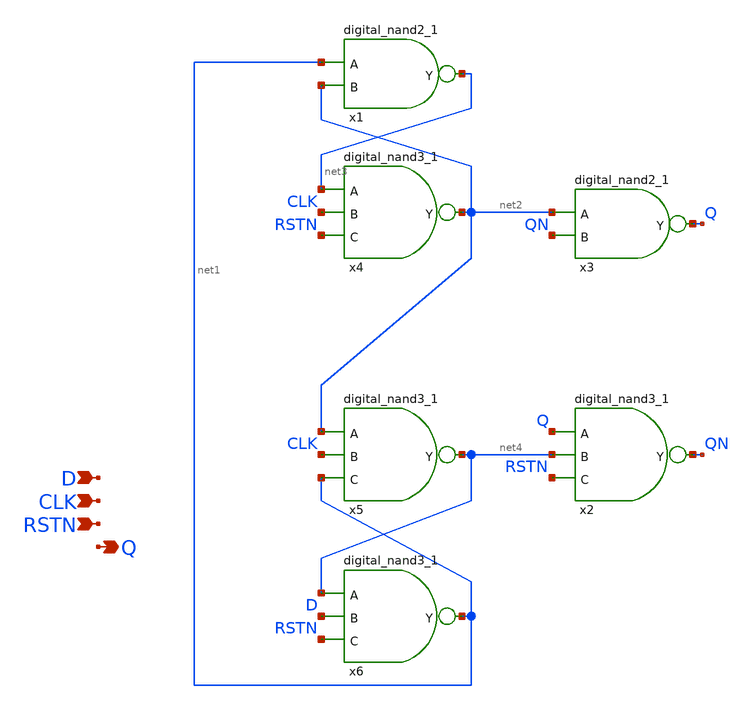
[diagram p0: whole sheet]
** sch_path: designs/libs/core_analog/digital/digital_dff.sch
**.subckt digital_dff D CLK Q RSTN
*.ipin D
*.ipin CLK
*.opin Q
*.ipin RSTN
x1 net1 net2 VDD VSS net3 digital_nand2_1
x3 net2 QN VDD VSS Q digital_nand2_1
x2 Q net4 RSTN VDD VSS QN digital_nand3_1
x4 net3 CLK RSTN VDD VSS net2 digital_nand3_1
x5 net2 CLK net1 VDD VSS net4 digital_nand3_1
x6 net4 D RSTN VDD VSS net1 digital_nand3_1
**.ends

* expanding   symbol:
*+  /foss/designs/sscs-chipathon2025-LNA/designs/libs/core_analog/digital/digital_nand2_1.sym # of pins=3
** sym_path: designs/libs/core_analog/digital/digital_nand2_1.sym
** sch_path: designs/libs/core_analog/digital/digital_nand2_1.sch
.subckt digital_nand2_1 A B VDD VSS Y
*.ipin A
*.ipin B
*.opin Y
XM3 Y A net1 VSS nfet_06v0 L=0.70u W=0.30u nf=1 ad='int((nf+1)/2) * W/nf * 0.18u' as='int((nf+2)/2) * W/nf * 0.18u'
+ pd='2*int((nf+1)/2) * (W/nf + 0.18u)' ps='2*int((nf+2)/2) * (W/nf + 0.18u)' nrd='0.18u / W' nrs='0.18u / W'
+ sa=0 sb=0 sd=0 m=1
XM4 net1 B VSS VSS nfet_06v0 L=0.70u W=0.30u nf=1 ad='int((nf+1)/2) * W/nf * 0.18u' as='int((nf+2)/2) * W/nf * 0.18u'
+ pd='2*int((nf+1)/2) * (W/nf + 0.18u)' ps='2*int((nf+2)/2) * (W/nf + 0.18u)' nrd='0.18u / W' nrs='0.18u / W'
+ sa=0 sb=0 sd=0 m=1
XM1 Y A VDD VDD pfet_06v0 L=0.55u W=0.90u nf=1 ad='int((nf+1)/2) * W/nf * 0.18u' as='int((nf+2)/2) * W/nf * 0.18u'
+ pd='2*int((nf+1)/2) * (W/nf + 0.18u)' ps='2*int((nf+2)/2) * (W/nf + 0.18u)' nrd='0.18u / W' nrs='0.18u / W'
+ sa=0 sb=0 sd=0 m=1
XM2 Y B VDD VDD pfet_06v0 L=0.55u W=0.90u nf=1 ad='int((nf+1)/2) * W/nf * 0.18u' as='int((nf+2)/2) * W/nf * 0.18u'
+ pd='2*int((nf+1)/2) * (W/nf + 0.18u)' ps='2*int((nf+2)/2) * (W/nf + 0.18u)' nrd='0.18u / W' nrs='0.18u / W'
+ sa=0 sb=0 sd=0 m=1
.ends


* expanding   symbol:
*+  /foss/designs/sscs-chipathon2025-LNA/designs/libs/core_analog/digital/digital_nand3_1.sym # of pins=4
** sym_path: designs/libs/core_analog/digital/digital_nand3_1.sym
** sch_path: designs/libs/core_analog/digital/digital_nand3_1.sch
.subckt digital_nand3_1 A B C VDD VSS Y
*.ipin A
*.ipin B
*.opin Y
*.ipin C
XM1 Y A VDD VDD pfet_06v0 L=0.55u W=0.90u nf=1 ad='int((nf+1)/2) * W/nf * 0.18u' as='int((nf+2)/2) * W/nf * 0.18u'
+ pd='2*int((nf+1)/2) * (W/nf + 0.18u)' ps='2*int((nf+2)/2) * (W/nf + 0.18u)' nrd='0.18u / W' nrs='0.18u / W'
+ sa=0 sb=0 sd=0 m=1
XM2 Y B VDD VDD pfet_06v0 L=0.55u W=0.90u nf=1 ad='int((nf+1)/2) * W/nf * 0.18u' as='int((nf+2)/2) * W/nf * 0.18u'
+ pd='2*int((nf+1)/2) * (W/nf + 0.18u)' ps='2*int((nf+2)/2) * (W/nf + 0.18u)' nrd='0.18u / W' nrs='0.18u / W'
+ sa=0 sb=0 sd=0 m=1
XM6 Y C VDD VDD pfet_06v0 L=0.55u W=0.90u nf=1 ad='int((nf+1)/2) * W/nf * 0.18u' as='int((nf+2)/2) * W/nf * 0.18u'
+ pd='2*int((nf+1)/2) * (W/nf + 0.18u)' ps='2*int((nf+2)/2) * (W/nf + 0.18u)' nrd='0.18u / W' nrs='0.18u / W'
+ sa=0 sb=0 sd=0 m=1
XM3 Y A net2 VSS nfet_06v0 L=0.70u W=0.30u nf=1 ad='int((nf+1)/2) * W/nf * 0.18u' as='int((nf+2)/2) * W/nf * 0.18u'
+ pd='2*int((nf+1)/2) * (W/nf + 0.18u)' ps='2*int((nf+2)/2) * (W/nf + 0.18u)' nrd='0.18u / W' nrs='0.18u / W'
+ sa=0 sb=0 sd=0 m=1
XM4 net2 B net1 VSS nfet_06v0 L=0.70u W=0.30u nf=1 ad='int((nf+1)/2) * W/nf * 0.18u' as='int((nf+2)/2) * W/nf * 0.18u'
+ pd='2*int((nf+1)/2) * (W/nf + 0.18u)' ps='2*int((nf+2)/2) * (W/nf + 0.18u)' nrd='0.18u / W' nrs='0.18u / W'
+ sa=0 sb=0 sd=0 m=1
XM5 net1 C VSS VSS nfet_06v0 L=0.70u W=0.30u nf=1 ad='int((nf+1)/2) * W/nf * 0.18u' as='int((nf+2)/2) * W/nf * 0.18u'
+ pd='2*int((nf+1)/2) * (W/nf + 0.18u)' ps='2*int((nf+2)/2) * (W/nf + 0.18u)' nrd='0.18u / W' nrs='0.18u / W'
+ sa=0 sb=0 sd=0 m=1
.ends

.end
